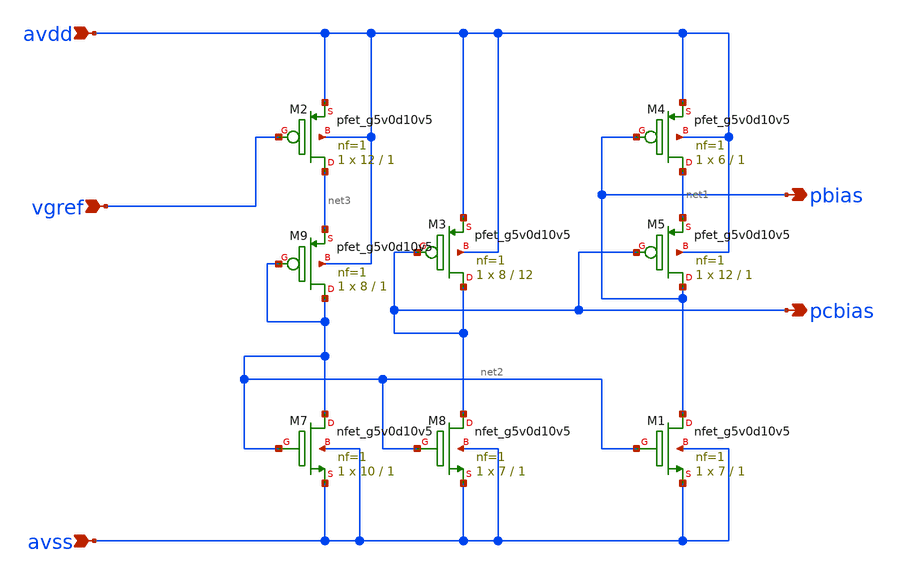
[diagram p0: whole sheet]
** sch_path: xschem/p_ibias_mirror.sch
**.subckt p_ibias_mirror avdd avss pbias pcbias vgref
*.ipin avdd
*.ipin avss
*.opin pbias
*.opin pcbias
*.ipin vgref
XM3 pcbias pcbias avdd avdd sky130_fd_pr__pfet_g5v0d10v5 L=12 W=8 nf=1 ad='int((nf+1)/2) * W/nf * 0.29'
+ as='int((nf+2)/2) * W/nf * 0.29' pd='2*int((nf+1)/2) * (W/nf + 0.29)' ps='2*int((nf+2)/2) * (W/nf + 0.29)'
+ nrd='0.29 / W' nrs='0.29 / W' sa=0 sb=0 sd=0 mult=1 m=1
XM4 net1 pbias avdd avdd sky130_fd_pr__pfet_g5v0d10v5 L=1 W=6 nf=1 ad='int((nf+1)/2) * W/nf * 0.29' as='int((nf+2)/2) * W/nf * 0.29'
+ pd='2*int((nf+1)/2) * (W/nf + 0.29)' ps='2*int((nf+2)/2) * (W/nf + 0.29)' nrd='0.29 / W' nrs='0.29 / W'
+ sa=0 sb=0 sd=0 mult=1 m=1
XM5 pbias pcbias net1 avdd sky130_fd_pr__pfet_g5v0d10v5 L=1 W=12 nf=1 ad='int((nf+1)/2) * W/nf * 0.29'
+ as='int((nf+2)/2) * W/nf * 0.29' pd='2*int((nf+1)/2) * (W/nf + 0.29)' ps='2*int((nf+2)/2) * (W/nf + 0.29)'
+ nrd='0.29 / W' nrs='0.29 / W' sa=0 sb=0 sd=0 mult=1 m=1
XM1 pbias net2 avss avss sky130_fd_pr__nfet_g5v0d10v5 L=1 W=7 nf=1 ad='int((nf+1)/2) * W/nf * 0.29' as='int((nf+2)/2) * W/nf * 0.29'
+ pd='2*int((nf+1)/2) * (W/nf + 0.29)' ps='2*int((nf+2)/2) * (W/nf + 0.29)' nrd='0.29 / W' nrs='0.29 / W'
+ sa=0 sb=0 sd=0 mult=1 m=1
XM2 net3 vgref avdd avdd sky130_fd_pr__pfet_g5v0d10v5 L=1 W=12 nf=1 ad='int((nf+1)/2) * W/nf * 0.29'
+ as='int((nf+2)/2) * W/nf * 0.29' pd='2*int((nf+1)/2) * (W/nf + 0.29)' ps='2*int((nf+2)/2) * (W/nf + 0.29)'
+ nrd='0.29 / W' nrs='0.29 / W' sa=0 sb=0 sd=0 mult=1 m=1
XM7 net2 net2 avss avss sky130_fd_pr__nfet_g5v0d10v5 L=1 W=10 nf=1 ad='int((nf+1)/2) * W/nf * 0.29' as='int((nf+2)/2) * W/nf * 0.29'
+ pd='2*int((nf+1)/2) * (W/nf + 0.29)' ps='2*int((nf+2)/2) * (W/nf + 0.29)' nrd='0.29 / W' nrs='0.29 / W'
+ sa=0 sb=0 sd=0 mult=1 m=1
XM8 pcbias net2 avss avss sky130_fd_pr__nfet_g5v0d10v5 L=1 W=7 nf=1 ad='int((nf+1)/2) * W/nf * 0.29'
+ as='int((nf+2)/2) * W/nf * 0.29' pd='2*int((nf+1)/2) * (W/nf + 0.29)' ps='2*int((nf+2)/2) * (W/nf + 0.29)'
+ nrd='0.29 / W' nrs='0.29 / W' sa=0 sb=0 sd=0 mult=1 m=1
XM9 net2 net2 net3 avdd sky130_fd_pr__pfet_g5v0d10v5 L=1 W=8 nf=1 ad='int((nf+1)/2) * W/nf * 0.29' as='int((nf+2)/2) * W/nf * 0.29'
+ pd='2*int((nf+1)/2) * (W/nf + 0.29)' ps='2*int((nf+2)/2) * (W/nf + 0.29)' nrd='0.29 / W' nrs='0.29 / W'
+ sa=0 sb=0 sd=0 mult=1 m=1
**.ends
.end
